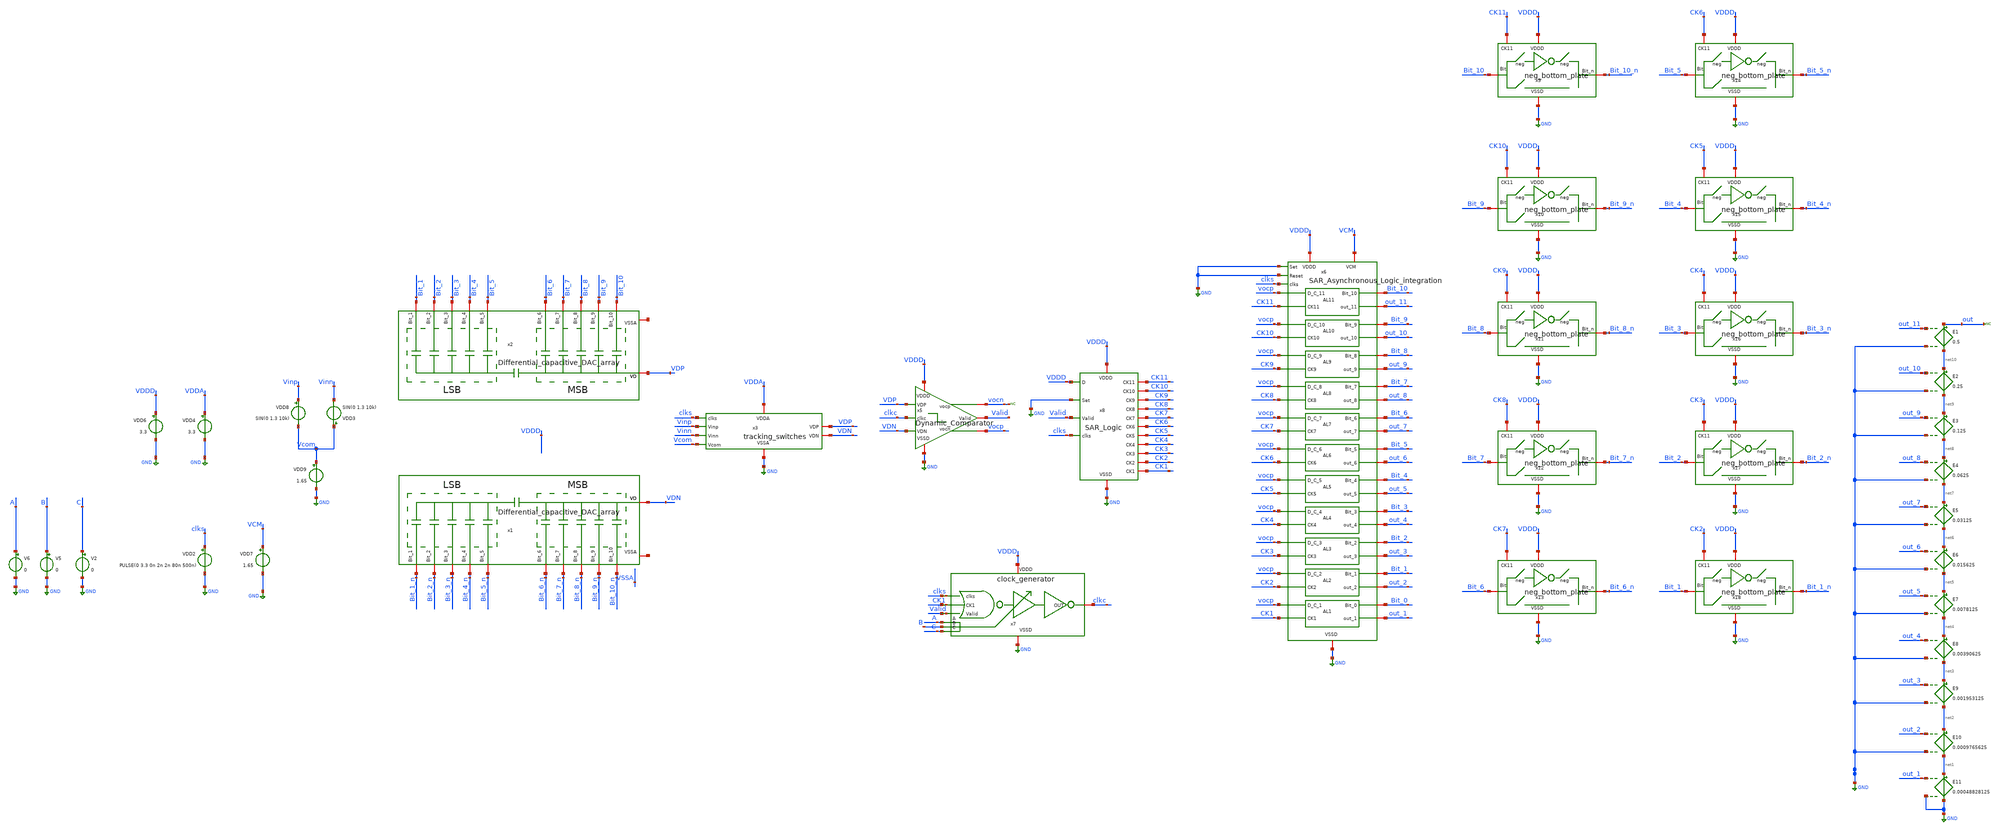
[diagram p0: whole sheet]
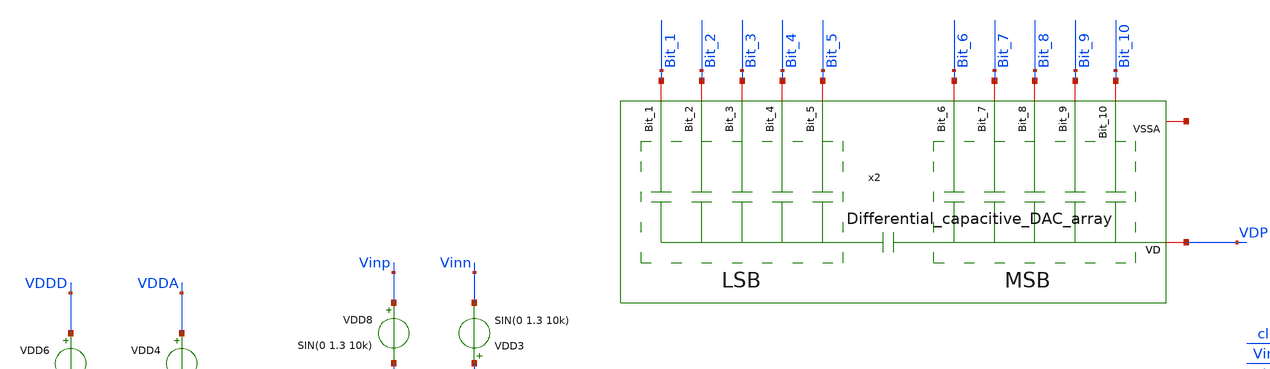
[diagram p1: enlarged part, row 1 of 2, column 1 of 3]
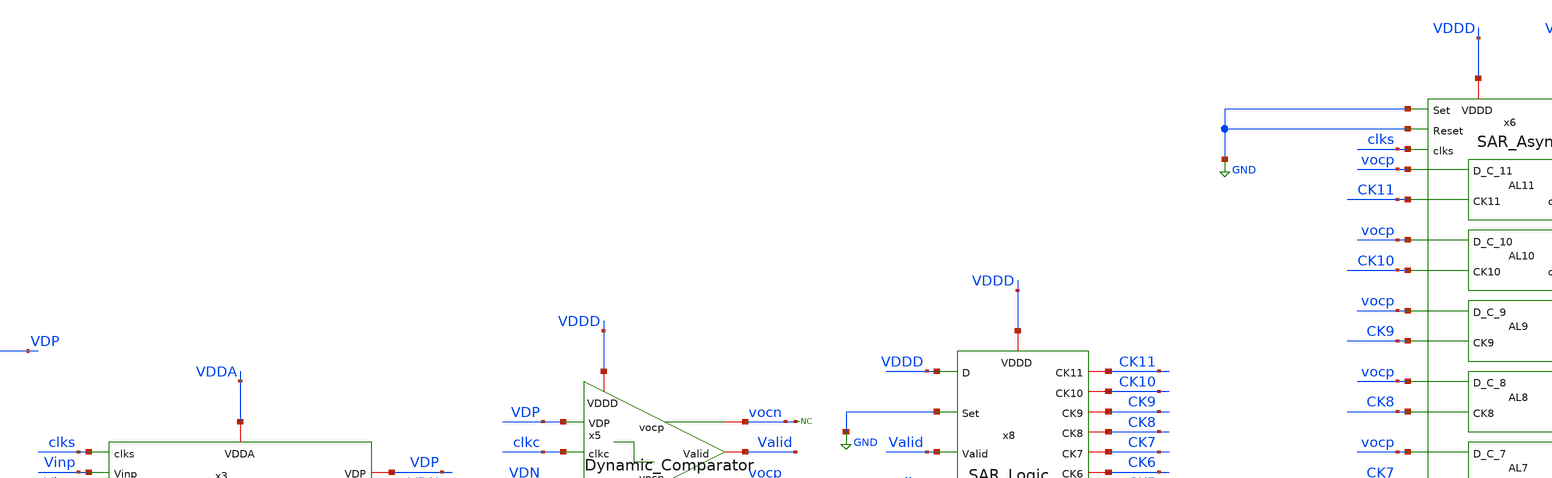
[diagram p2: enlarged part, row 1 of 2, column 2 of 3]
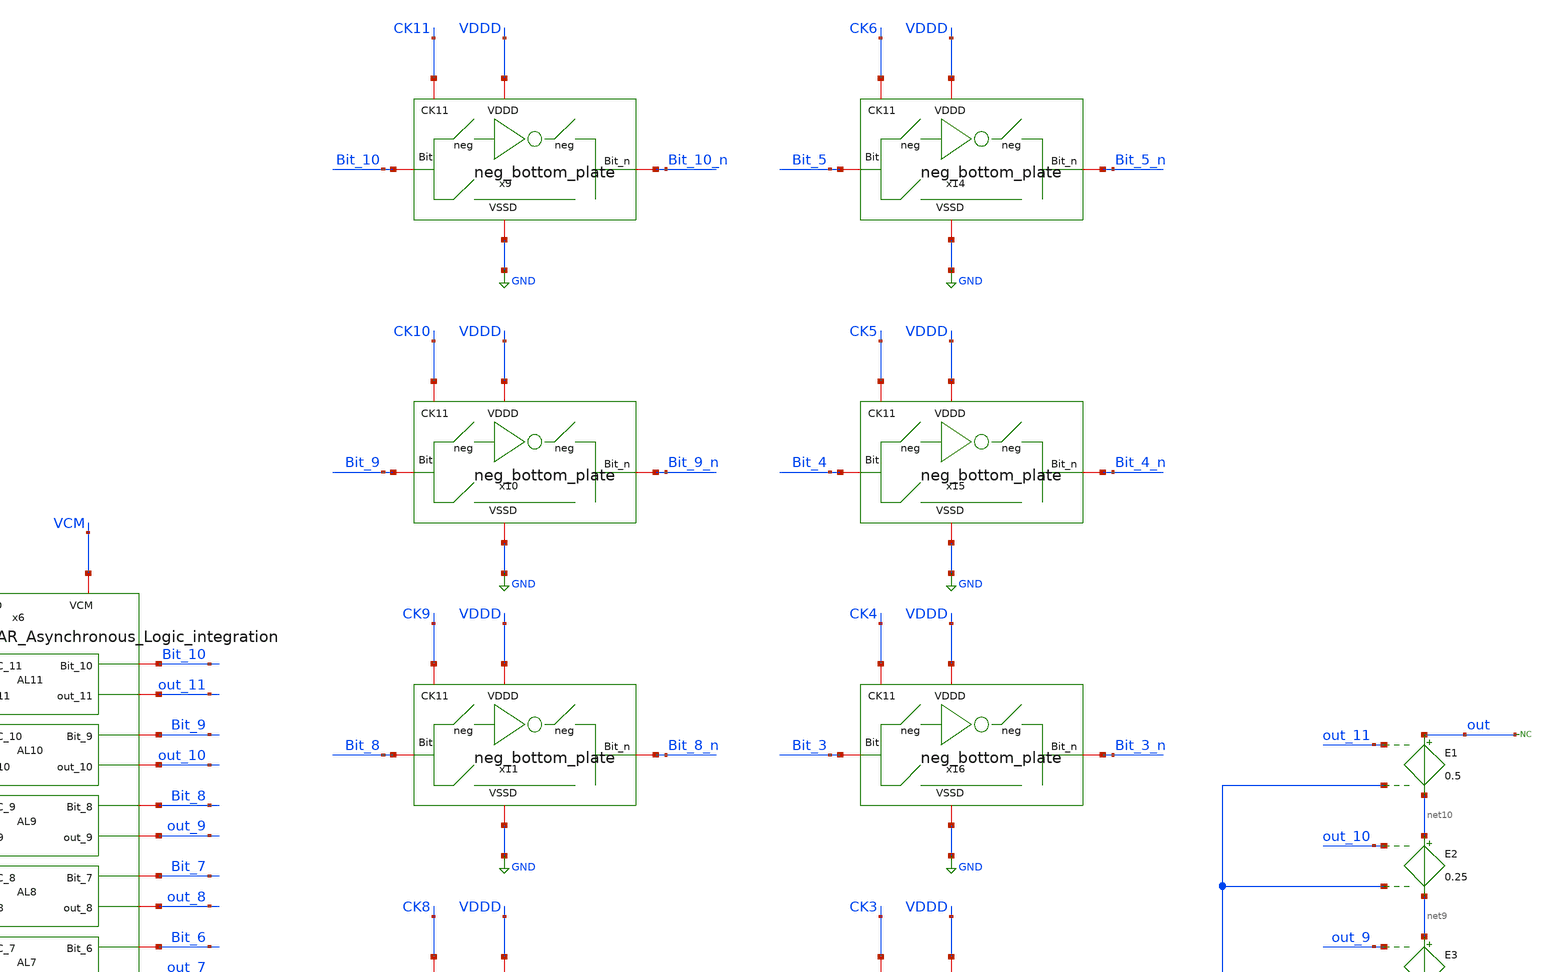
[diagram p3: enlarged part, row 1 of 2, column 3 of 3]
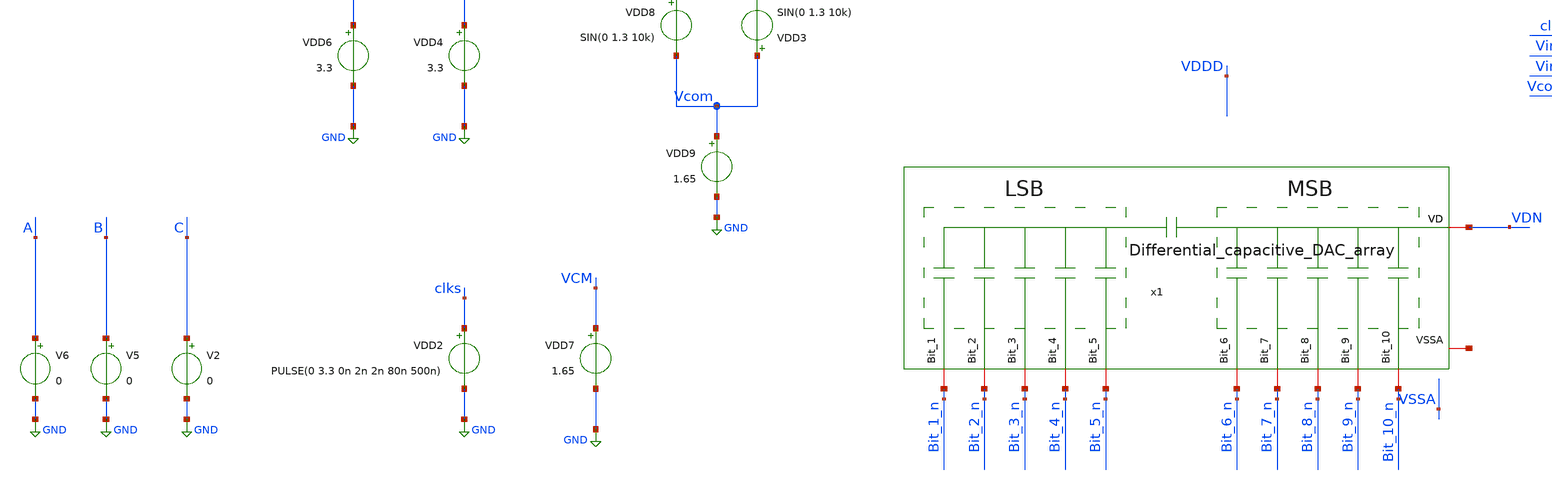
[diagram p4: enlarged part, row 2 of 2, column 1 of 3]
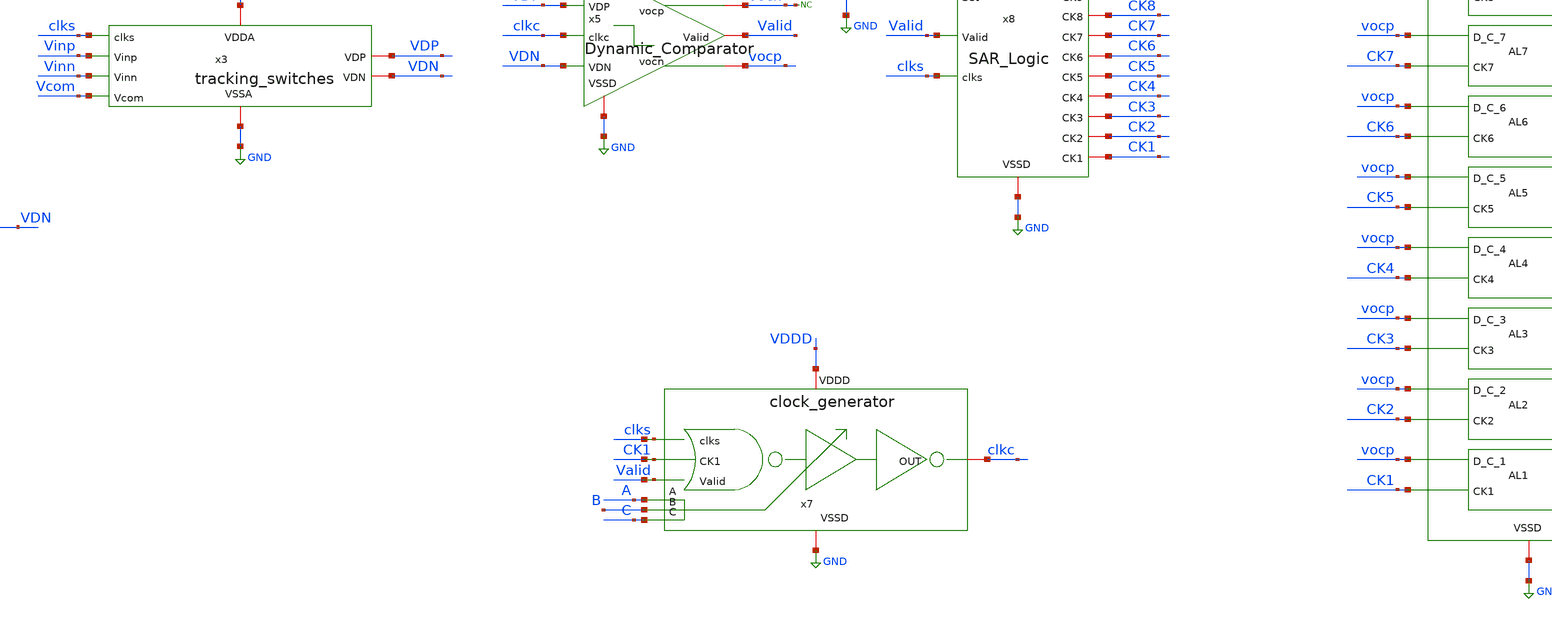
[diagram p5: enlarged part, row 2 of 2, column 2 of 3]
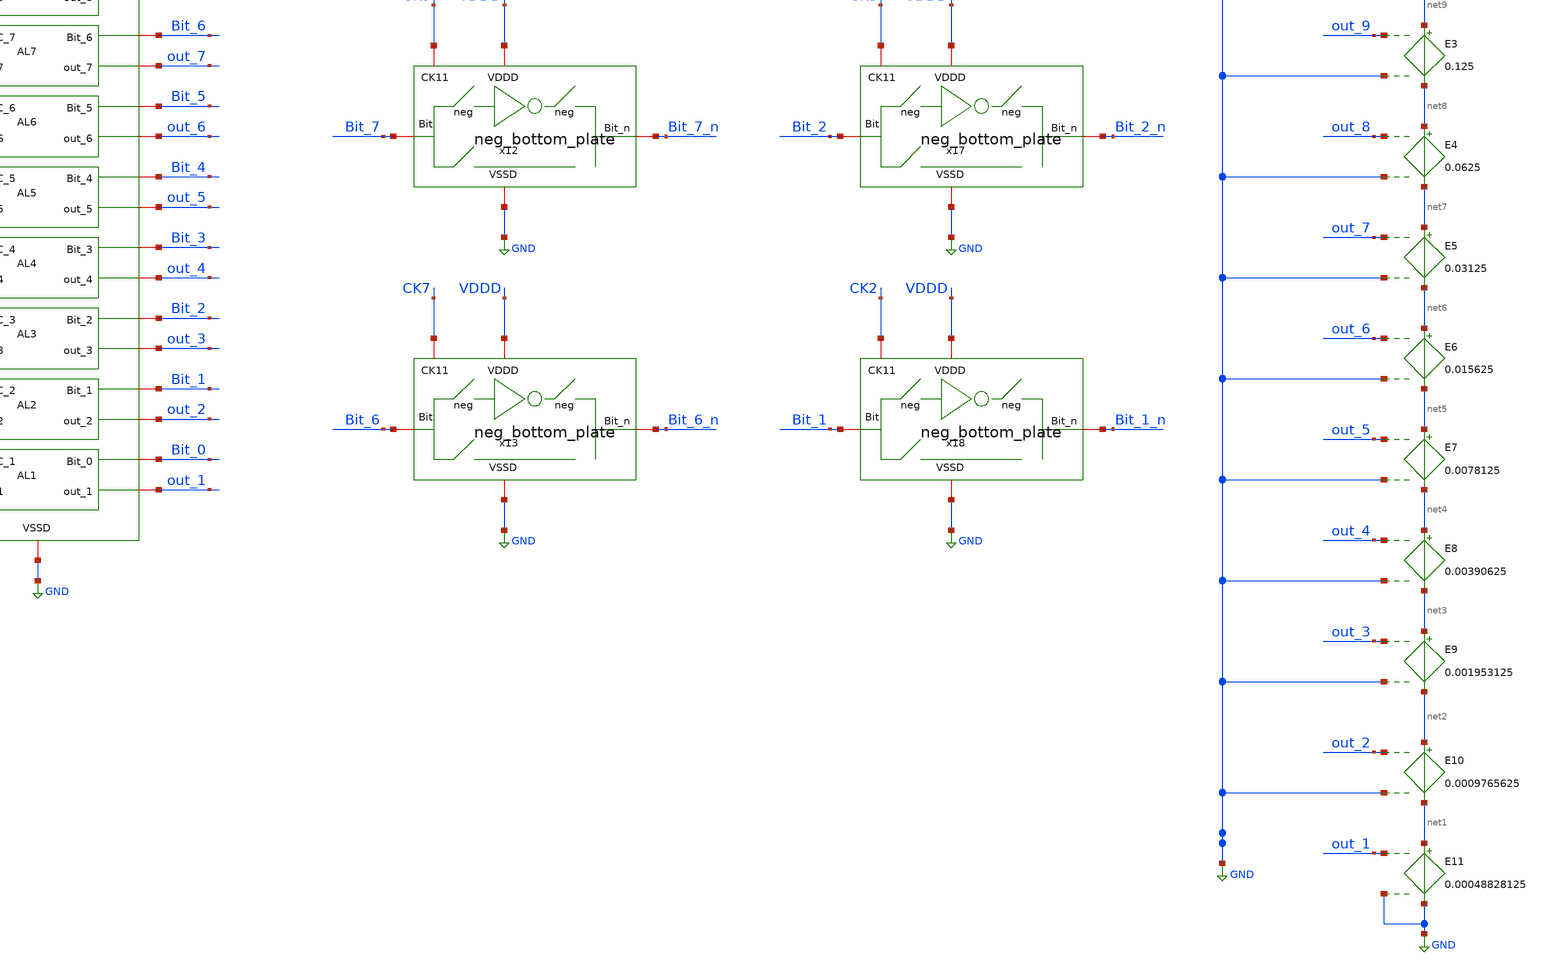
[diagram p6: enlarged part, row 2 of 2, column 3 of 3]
** sch_path: SAR_ADC/integration/integration_tb.sch
**.subckt integration_tb
x1 VDN Bit_3_n Bit_8_n Bit_5_n Bit_6_n Bit_7_n Bit_4_n Bit_9_n Bit_10_n Bit_2_n Bit_1_n net11
+ Differential_capacitive_DAC_array
x2 VDP Bit_3 Bit_8 Bit_5 Bit_6 Bit_7 Bit_4 Bit_9 Bit_10 Bit_2 Bit_1 net12
+ Differential_capacitive_DAC_array
x3 VDP VDN VDDA GND clks Vinp Vinn Vcom tracking_switches
x5 vocn vocp VDDD GND VDP VDN Valid clkc Dynamic_Comparator
x6 VDDD Bit_10 vocp GND CK11 VCM out_11 GND GND clks Bit_9 vocp CK10 out_10 Bit_8 vocp CK9 out_9
+ Bit_7 vocp CK8 out_8 Bit_6 vocp CK7 out_7 Bit_5 vocp CK6 out_6 Bit_4 vocp CK5 out_5 Bit_3 vocp CK4 out_4
+ Bit_2 vocp CK3 out_3 Bit_1 vocp CK2 out_2 Bit_0 vocp CK1 out_1 SAR_Asynchronous_Logic_integration
x7 clkc VDDD GND clks CK1 Valid A B C clock_generator
VDD4 VDDA GND 3.3
VDD3 Vcom Vinn SIN(0 1.3 10k)
VDD6 VDDD GND 3.3
VDD2 clks GND PULSE(0 3.3 0n 2n 2n 80n 500n)
VDD7 VCM GND 1.65
x8 CK11 VDDD CK1 CK6 GND CK10 CK5 CK9 CK4 clks CK8 CK3 Valid CK2 CK7 GND VDDD SAR_Logic
V2 C GND 0
V5 B GND 0
V6 A GND 0
x9 VDDD GND CK11 Bit_10 Bit_10_n neg_bottom_plate
x10 VDDD GND CK10 Bit_9 Bit_9_n neg_bottom_plate
x11 VDDD GND CK9 Bit_8 Bit_8_n neg_bottom_plate
x12 VDDD GND CK8 Bit_7 Bit_7_n neg_bottom_plate
x13 VDDD GND CK7 Bit_6 Bit_6_n neg_bottom_plate
x14 VDDD GND CK6 Bit_5 Bit_5_n neg_bottom_plate
x15 VDDD GND CK5 Bit_4 Bit_4_n neg_bottom_plate
x16 VDDD GND CK4 Bit_3 Bit_3_n neg_bottom_plate
x17 VDDD GND CK3 Bit_2 Bit_2_n neg_bottom_plate
x18 VDDD GND CK2 Bit_1 Bit_1_n neg_bottom_plate
E1 out net10 out_11 GND 0.5
E2 net10 net9 out_10 GND 0.25
E3 net9 net8 out_9 GND 0.125
E4 net8 net7 out_8 GND 0.0625
E5 net7 net6 out_7 GND 0.03125
E6 net6 net5 out_6 GND 0.015625
E7 net5 net4 out_5 GND 0.0078125
E8 net4 net3 out_4 GND 0.00390625
E9 net3 net2 out_3 GND 0.001953125
E10 net2 net1 out_2 GND 0.0009765625
E11 net1 GND out_1 GND 0.00048828125
* noconn out
* noconn vocn
VDD8 Vinp Vcom SIN(0 1.3 10k)
VDD9 Vcom GND 1.65
**** begin user architecture code



*Parameters

.options TEMP = 50
.lib /home/gf180/Documents/gf180/pdk/gf180mcuD/libs.tech/ngspice/sm141064.ngspice typical
.lib /home/gf180/Documents/gf180/pdk/gf180mcuD/libs.tech/ngspice/sm141064.ngspice cap_mim

.lib /home/gf180/Documents/gf180/pdk/gf180mcuD/libs.tech/ngspice/sm141064.ngspice mimcap_statistical
.include /home/gf180/Documents/gf180/pdk/gf180mcuD/libs.tech/ngspice/design.ngspice

*Data to save
.save v(Vinp)
*.save v(VDP)
.save v(Vinn)
*.save v(VDN)
*.save v(clkc)
*.save v(x5.aN)
*.save v(x5.aP)
*.save v(x5.dN)
*.save v(x5.dP)

*.save v(clks)
*.save v(CK1)
*.save v(Valid)
*.save v(CK11)
*.save v(CK10)
*.save v(CK9)
*.save v(CK8)
*.save v(CK7)
*.save v(CK6)
*.save v(CK5)
*.save v(CK4)
*.save v(CK3)
*.save v(CK2)
*.save v(CK1)
*.save v(Bit_10)
*.save v(Bit_10_n)
*.save v(Bit_9)
*.save v(Bit_9_n)
*.save v(Bit_8)
*.save v(Bit_8_n)
*.save v(Bit_7)
*.save v(Bit_7_n)
*.save v(Bit_6)
*.save v(Bit_6_n)
*.save v(Bit_5)
*.save v(Bit_5_n)
*.save v(Bit_4)
*.save v(Bit_4_n)
*.save v(Bit_3)
*.save v(Bit_3_n)
*.save v(Bit_2)
*.save v(Bit_2_n)
*.save v(Bit_1)
*.save v(Bit_1_n)
*.save v(vocp)
*.save v(vocn)
.save v(out)

* Simulation
.control
tran 500n 100u
*setplot dc1
*let vout_diff = VDP - VDN
let vin_diff = Vinp - Vinn
*plot v(Bit_10_n)+48 v(Bit_10)+48 v(Bit_9_n)+44 v(Bit_9)+44 v(Bit_8_n)+40 v(Bit_8)+40 v(Bit_7_n)+36
*+ v(Bit_7)+36 v(Bit_6_n)+32 v(Bit_6)+32 v(Bit_5_n)+28 v(Bit_5)+28 v(Bit_4_n)+24 v(Bit_4)+24 v(Bit_3_n)+20
*+ v(Bit_3)+20 v(Bit_2_n)+16 v(Bit_2)+16 v(Bit_1_n)+12 v(Bit_1)+12 v(clks)+8 v(Valid)+4 v(vin_diff) v(vout_diff)
*plot v(clks)+8 v(Vinp)+4 v(VDP)+4 v(Vinn) v(VDN)
*set filetype=ascii
*plot v(clks)+12 v(Valid)+8 v(vin_diff)+4 v(vout_diff)+4 v(Vinp) v(out)
plot (vin_diff) v(out)

*setplot dc2
*plot v(clks)+8 v(Vinp)+4 v(VDP)

*setplot dc3
*plot v(clkc)+20 v(VDP)+16 v(VDN)+12 v(vocp)+8 v(vocn)+4 v(Valid)

*setplot dc4
*plot v(Valid)+48 v(clks)+44 v(CK11)+40 v(CK10)+36 v(CK9)+32 v(CK8)+28 v(CK7)+24 v(CK6)+20 v(CK5)+16
*+ v(CK4)+12 v(CK3)+8 v(CK2)+4 v(CK1)

*setplot dc1
*plot v(VDP)+20 v(VDN)+20 v(clkc)+16 v(x5.aN)+12 v(x5.aP)+8 v(x5.dP)+4 v(x5.dN)

set filetype = ascii
write integration_tb_dc.raw

reset
unset filetype
op
save all
write integration_tb.raw


.endc
.end


**** end user architecture code
**.ends
.GLOBAL GND
.end
